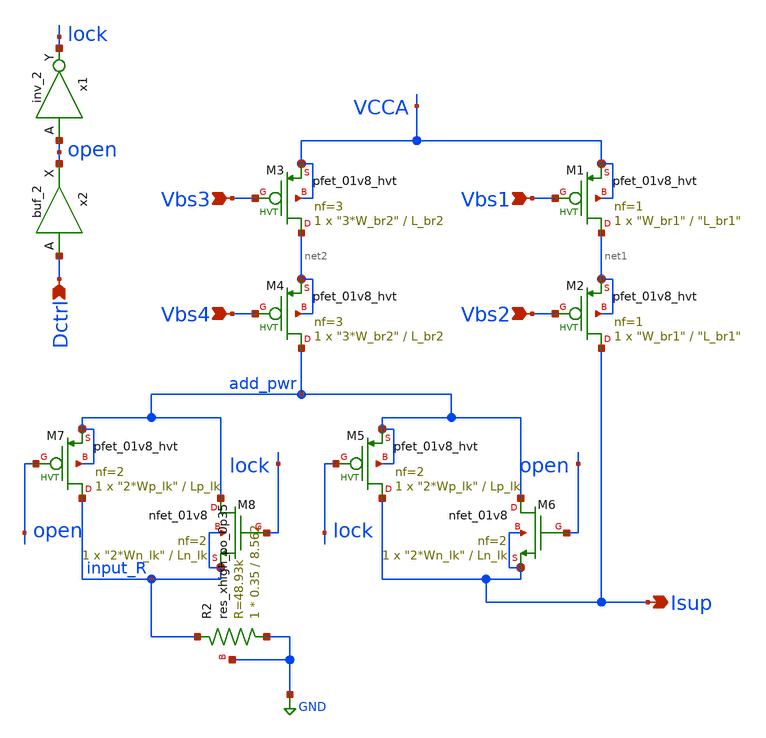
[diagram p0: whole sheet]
** sch_path: xschem/lib_dco/dco_idac.sch
**.subckt dco_idac Vbs3 Vbs4 Vbs1 Vbs2 Isup Dctrl
*.ipin Vbs3
*.ipin Vbs4
*.ipin Vbs1
*.ipin Vbs2
*.opin Isup
*.ipin Dctrl
x1 open GND GND VCCD VCCD lock sky130_fd_sc_hd__inv_2
XM1 net1 Vbs1 VCCA VCCA sky130_fd_pr__pfet_01v8_hvt L="L_br1" W="W_br1" nf=1 ad='int((nf+1)/2) * W/nf * 0.29'
+ as='int((nf+2)/2) * W/nf * 0.29' pd='2*int((nf+1)/2) * (W/nf + 0.29)' ps='2*int((nf+2)/2) * (W/nf + 0.29)'
+ nrd='0.29 / W' nrs='0.29 / W' sa=0 sb=0 sd=0 mult=1 m=1
XM2 Isup Vbs2 net1 net1 sky130_fd_pr__pfet_01v8_hvt L="L_br1" W="W_br1" nf=1 ad='int((nf+1)/2) * W/nf * 0.29'
+ as='int((nf+2)/2) * W/nf * 0.29' pd='2*int((nf+1)/2) * (W/nf + 0.29)' ps='2*int((nf+2)/2) * (W/nf + 0.29)'
+ nrd='0.29 / W' nrs='0.29 / W' sa=0 sb=0 sd=0 mult=1 m=1
x2 Dctrl GND GND VCCD VCCD open sky130_fd_sc_hd__buf_2
XM3 net2 Vbs3 VCCA VCCA sky130_fd_pr__pfet_01v8_hvt L=L_br2 W="3*W_br2" nf=3 ad='int((nf+1)/2) * W/nf * 0.29'
+ as='int((nf+2)/2) * W/nf * 0.29' pd='2*int((nf+1)/2) * (W/nf + 0.29)' ps='2*int((nf+2)/2) * (W/nf + 0.29)'
+ nrd='0.29 / W' nrs='0.29 / W' sa=0 sb=0 sd=0 mult=1 m=1
XM4 add_pwr Vbs4 net2 net2 sky130_fd_pr__pfet_01v8_hvt L=L_br2 W="3*W_br2" nf=3 ad='int((nf+1)/2) * W/nf * 0.29'
+ as='int((nf+2)/2) * W/nf * 0.29' pd='2*int((nf+1)/2) * (W/nf + 0.29)' ps='2*int((nf+2)/2) * (W/nf + 0.29)'
+ nrd='0.29 / W' nrs='0.29 / W' sa=0 sb=0 sd=0 mult=1 m=1
XM5 Isup lock add_pwr add_pwr sky130_fd_pr__pfet_01v8_hvt L=Lp_lk W="2*Wp_lk" nf=2 ad='int((nf+1)/2) * W/nf * 0.29'
+ as='int((nf+2)/2) * W/nf * 0.29' pd='2*int((nf+1)/2) * (W/nf + 0.29)' ps='2*int((nf+2)/2) * (W/nf + 0.29)'
+ nrd='0.29 / W' nrs='0.29 / W' sa=0 sb=0 sd=0 mult=1 m=1
XM6 add_pwr open Isup Isup sky130_fd_pr__nfet_01v8 L=Ln_lk W="2*Wn_lk" nf=2 ad='int((nf+1)/2) * W/nf * 0.29'
+ as='int((nf+2)/2) * W/nf * 0.29' pd='2*int((nf+1)/2) * (W/nf + 0.29)' ps='2*int((nf+2)/2) * (W/nf + 0.29)'
+ nrd='0.29 / W' nrs='0.29 / W' sa=0 sb=0 sd=0 mult=1 m=1
XM7 input_R open add_pwr add_pwr sky130_fd_pr__pfet_01v8_hvt L=Lp_lk W="2*Wp_lk" nf=2 ad='int((nf+1)/2) * W/nf * 0.29'
+ as='int((nf+2)/2) * W/nf * 0.29' pd='2*int((nf+1)/2) * (W/nf + 0.29)' ps='2*int((nf+2)/2) * (W/nf + 0.29)'
+ nrd='0.29 / W' nrs='0.29 / W' sa=0 sb=0 sd=0 mult=1 m=1
XM8 add_pwr lock input_R input_R sky130_fd_pr__nfet_01v8 L=Ln_lk W="2*Wn_lk" nf=2 ad='int((nf+1)/2) * W/nf * 0.29'
+ as='int((nf+2)/2) * W/nf * 0.29' pd='2*int((nf+1)/2) * (W/nf + 0.29)' ps='2*int((nf+2)/2) * (W/nf + 0.29)'
+ nrd='0.29 / W' nrs='0.29 / W' sa=0 sb=0 sd=0 mult=1 m=1
XR2 GND input_R GND sky130_fd_pr__res_xhigh_po_0p35 L=8.562 mult=1 m=1
**.ends
.GLOBAL GND
.end
